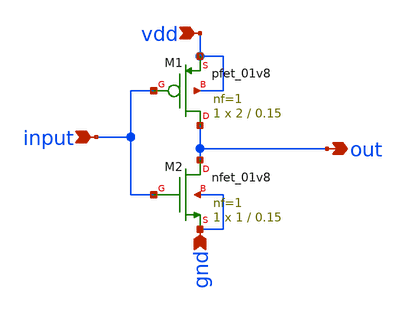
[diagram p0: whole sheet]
** sch_path: extra_stuff/inv.sch
**.subckt inv input vdd gnd out
*.ipin input
*.ipin vdd
*.ipin gnd
*.opin out
XM1 out input vdd vdd sky130_fd_pr__pfet_01v8 L=0.15 W=2 nf=1 ad='int((1 + 1)/2) * 2 / 1 * 0.29' as='int((1 + 2)/2) * 2 / 1 * 0.29'
+ pd='2*int((1 + 1)/2) * (2 / 1 + 0.29)' ps='2*int((1 + 2)/2) * (2 / 1 + 0.29)' nrd='0.29 / 2 ' nrs='0.29 / 2 '
+ sa=0 sb=0 sd=0 mult=1 m=1
XM2 out input gnd gnd sky130_fd_pr__nfet_01v8 L=0.15 W=1 nf=1 ad='int((1 + 1)/2) * 1 / 1 * 0.29' as='int((1 + 2)/2) * 1 / 1 * 0.29'
+ pd='2*int((1 + 1)/2) * (1 / 1 + 0.29)' ps='2*int((1 + 2)/2) * (1 / 1 + 0.29)' nrd='0.29 / 1 ' nrs='0.29 / 1 '
+ sa=0 sb=0 sd=0 mult=1 m=1
**.ends
.end
